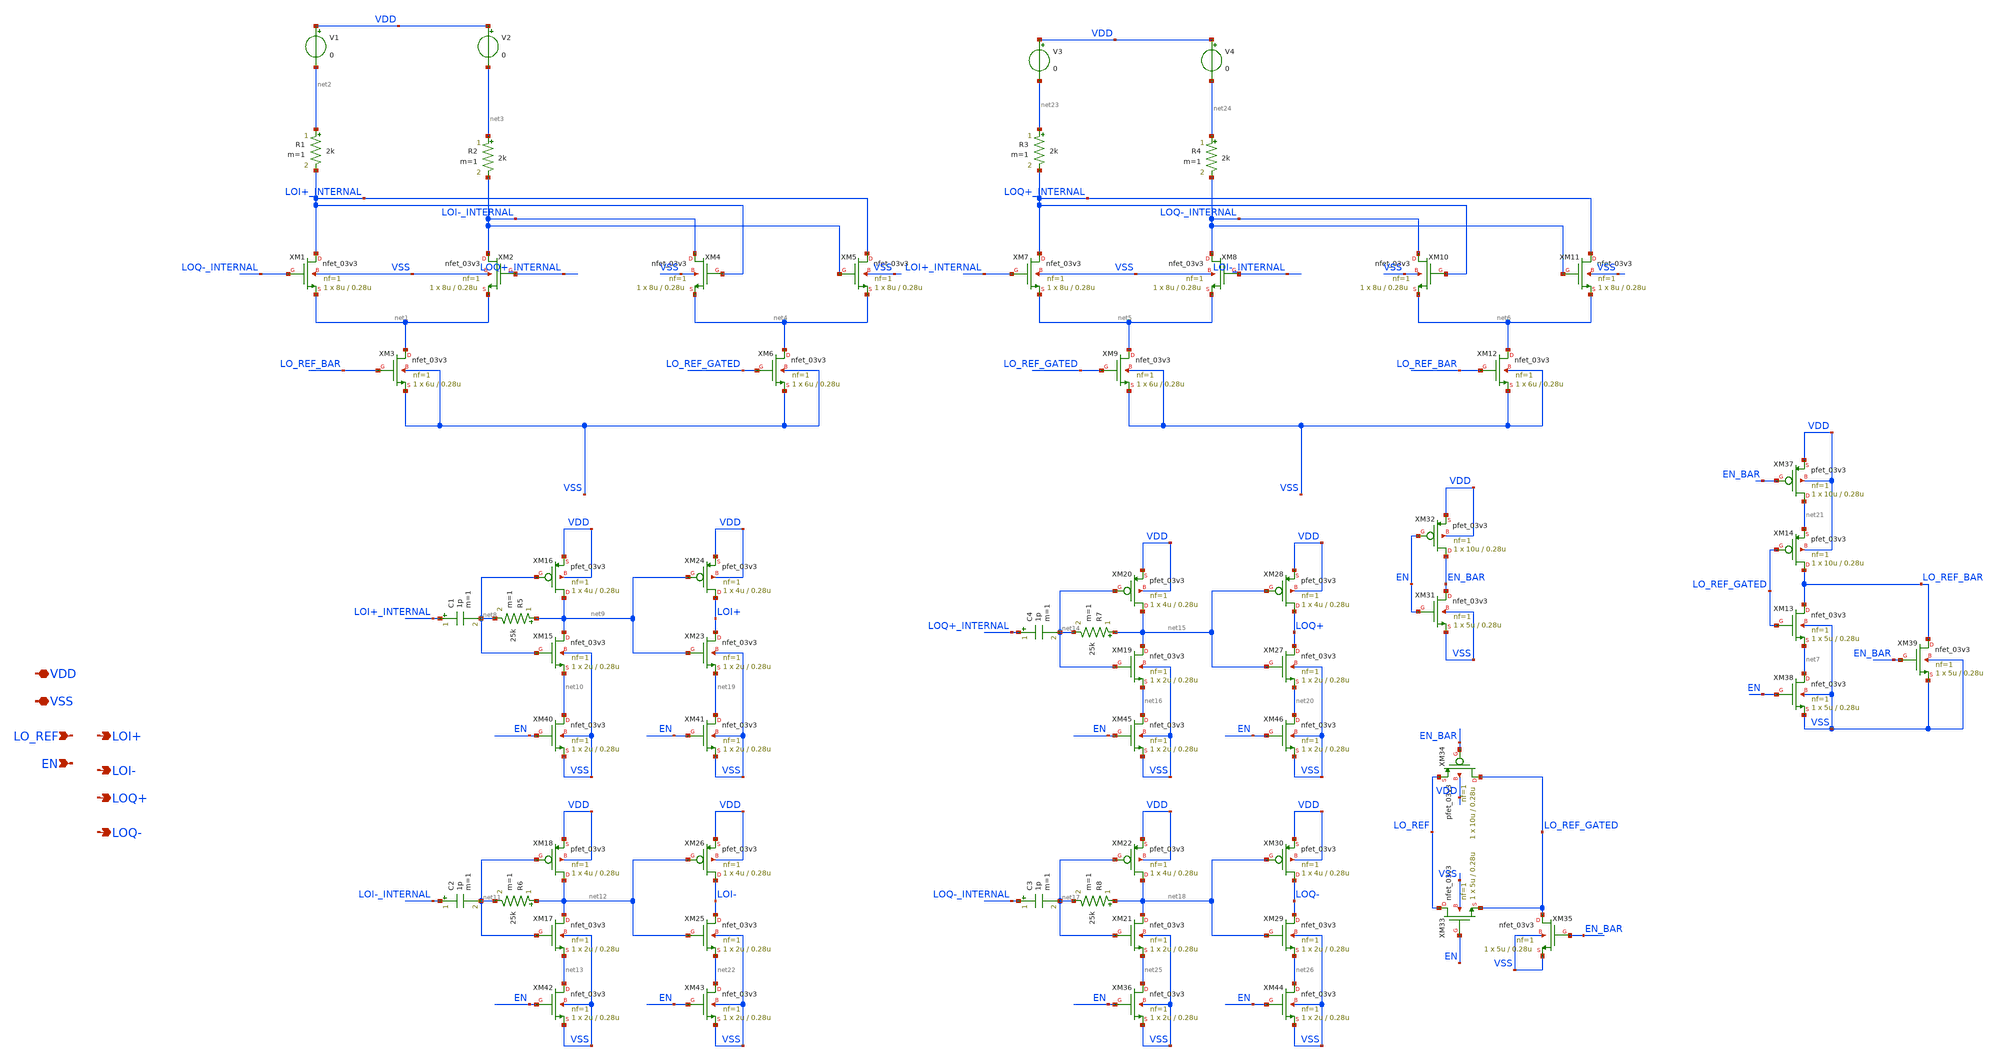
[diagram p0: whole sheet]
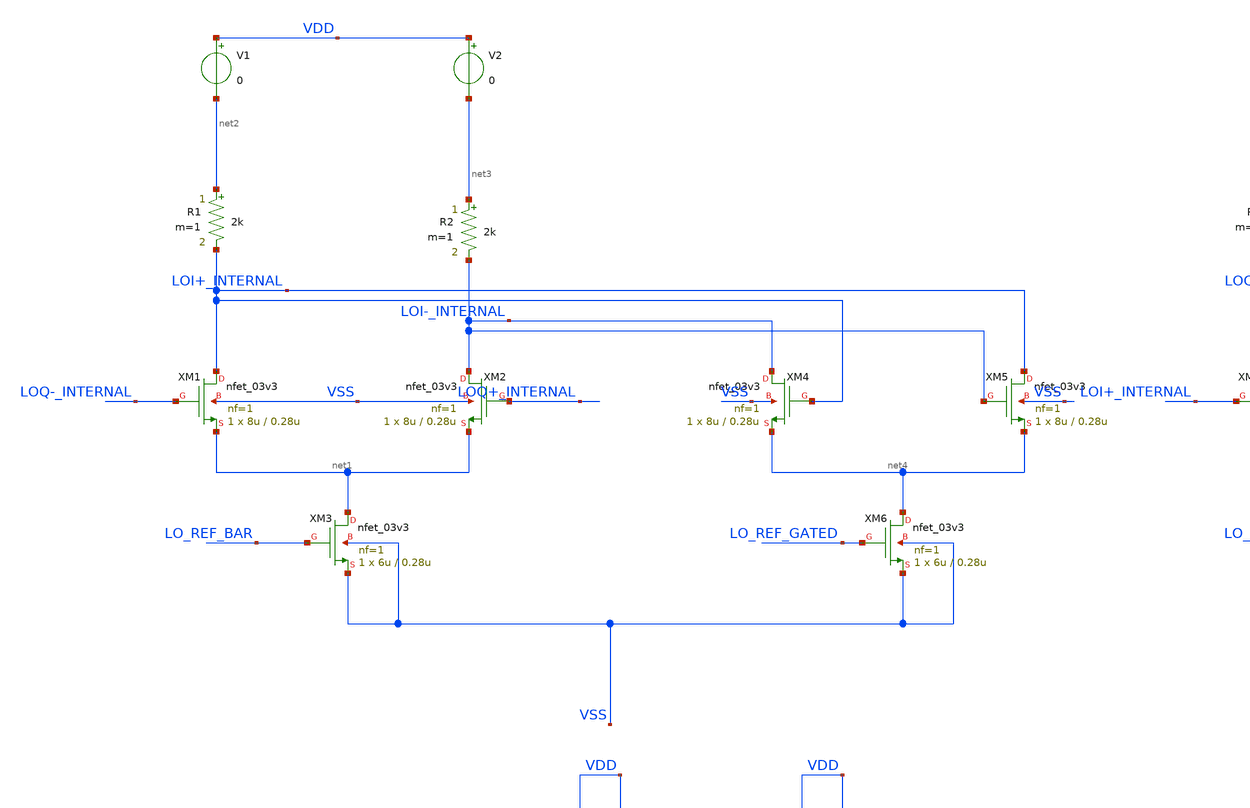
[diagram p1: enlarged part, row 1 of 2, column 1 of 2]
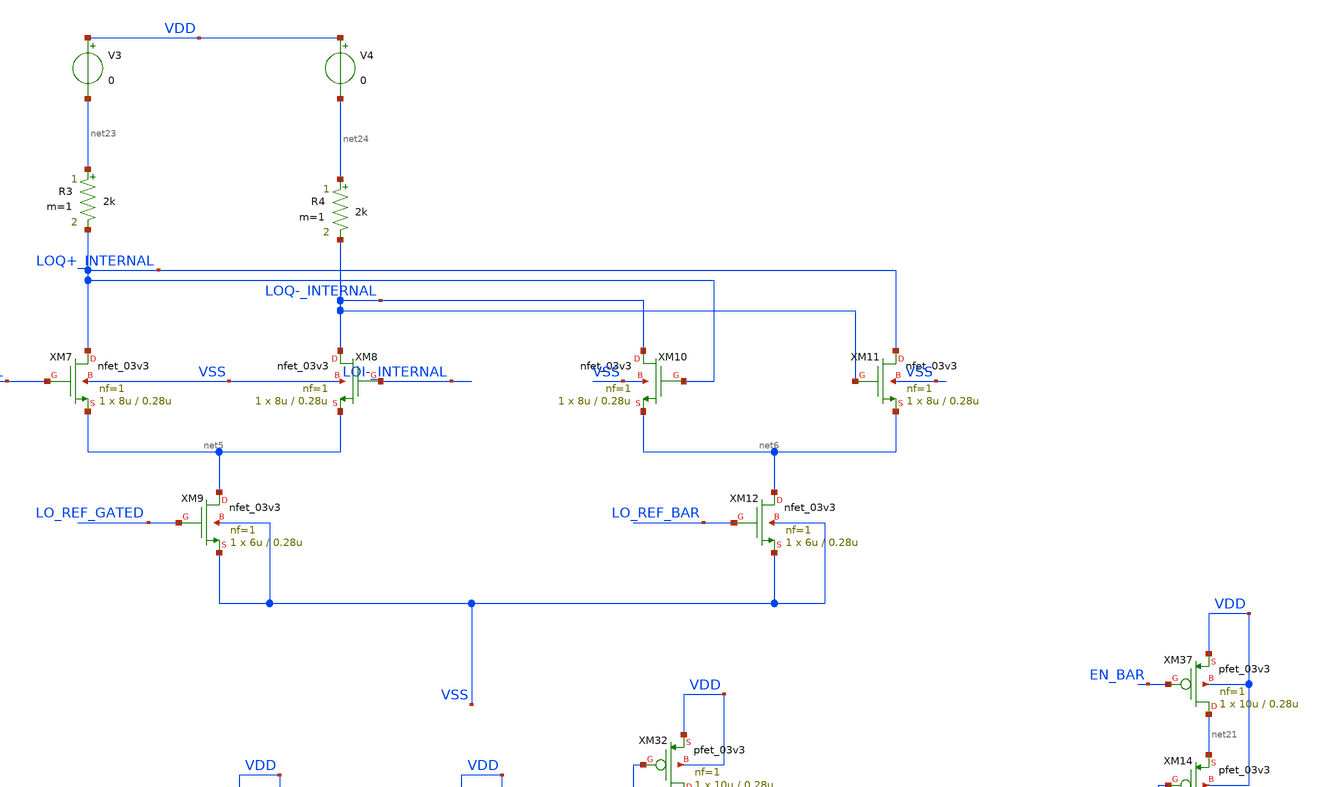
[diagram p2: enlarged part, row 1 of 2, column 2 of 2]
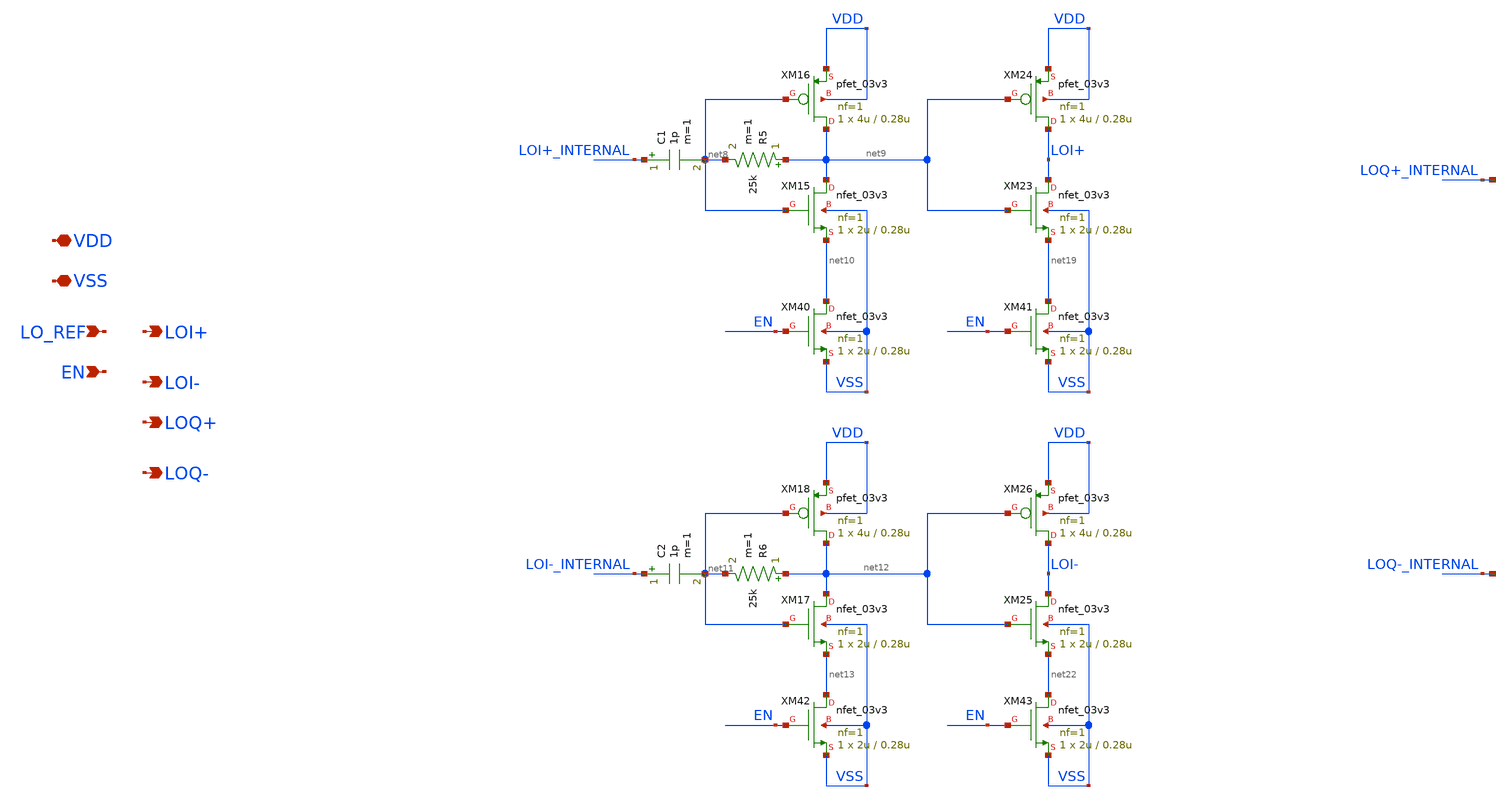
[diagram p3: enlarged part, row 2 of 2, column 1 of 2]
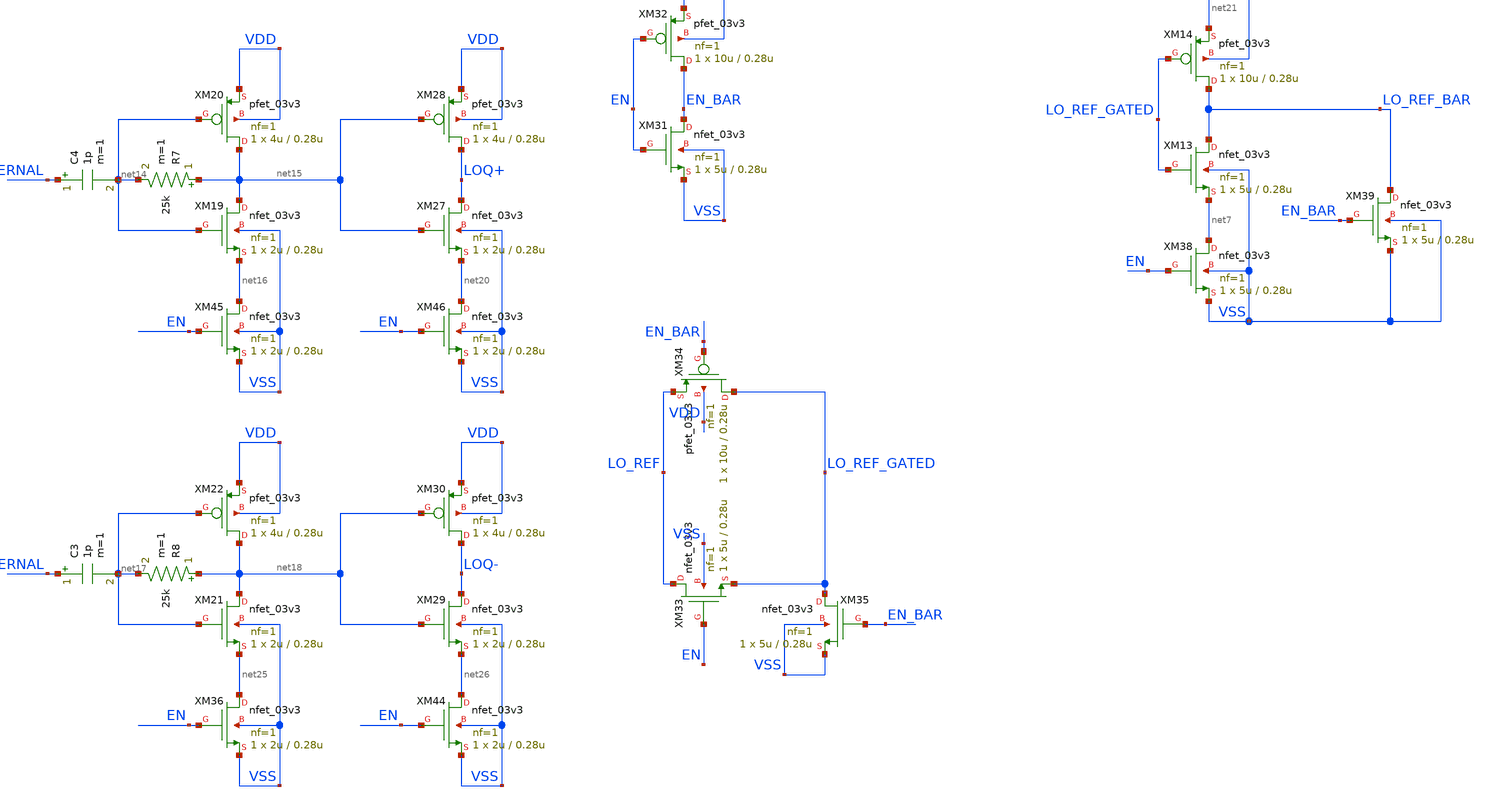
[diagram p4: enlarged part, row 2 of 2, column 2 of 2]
** sch_path: designs/divider/schematic/divider_ideal_passives.sch
**.subckt divider_ideal_passives VDD VSS LO_REF LOI+ LOI- LOQ+ LOQ- EN
*.iopin VDD
*.iopin VSS
*.ipin LO_REF
*.opin LOI+
*.opin LOI-
*.opin LOQ+
*.opin LOQ-
*.ipin EN
XM1 LOI+_INTERNAL LOQ-_INTERNAL net1 VSS nfet_03v3 L=0.28u W=8u nf=1 ad='int((nf+1)/2) * W/nf * 0.18u'
+ as='int((nf+2)/2) * W/nf * 0.18u' pd='2*int((nf+1)/2) * (W/nf + 0.18u)' ps='2*int((nf+2)/2) * (W/nf + 0.18u)'
+ nrd='0.18u / W' nrs='0.18u / W' sa=0 sb=0 sd=0 m=1
XM2 LOI-_INTERNAL LOQ+_INTERNAL net1 VSS nfet_03v3 L=0.28u W=8u nf=1 ad='int((nf+1)/2) * W/nf * 0.18u'
+ as='int((nf+2)/2) * W/nf * 0.18u' pd='2*int((nf+1)/2) * (W/nf + 0.18u)' ps='2*int((nf+2)/2) * (W/nf + 0.18u)'
+ nrd='0.18u / W' nrs='0.18u / W' sa=0 sb=0 sd=0 m=1
XM3 net1 LO_REF_BAR VSS VSS nfet_03v3 L=0.28u W=6u nf=1 ad='int((nf+1)/2) * W/nf * 0.18u' as='int((nf+2)/2) * W/nf * 0.18u'
+ pd='2*int((nf+1)/2) * (W/nf + 0.18u)' ps='2*int((nf+2)/2) * (W/nf + 0.18u)' nrd='0.18u / W' nrs='0.18u / W'
+ sa=0 sb=0 sd=0 m=1
R1 net2 LOI+_INTERNAL 2k m=1
R2 net3 LOI-_INTERNAL 2k m=1
XM4 LOI-_INTERNAL LOI+_INTERNAL net4 VSS nfet_03v3 L=0.28u W=8u nf=1 ad='int((nf+1)/2) * W/nf * 0.18u'
+ as='int((nf+2)/2) * W/nf * 0.18u' pd='2*int((nf+1)/2) * (W/nf + 0.18u)' ps='2*int((nf+2)/2) * (W/nf + 0.18u)'
+ nrd='0.18u / W' nrs='0.18u / W' sa=0 sb=0 sd=0 m=1
XM5 LOI+_INTERNAL LOI-_INTERNAL net4 VSS nfet_03v3 L=0.28u W=8u nf=1 ad='int((nf+1)/2) * W/nf * 0.18u'
+ as='int((nf+2)/2) * W/nf * 0.18u' pd='2*int((nf+1)/2) * (W/nf + 0.18u)' ps='2*int((nf+2)/2) * (W/nf + 0.18u)'
+ nrd='0.18u / W' nrs='0.18u / W' sa=0 sb=0 sd=0 m=1
XM6 net4 LO_REF_GATED VSS VSS nfet_03v3 L=0.28u W=6u nf=1 ad='int((nf+1)/2) * W/nf * 0.18u' as='int((nf+2)/2) * W/nf * 0.18u'
+ pd='2*int((nf+1)/2) * (W/nf + 0.18u)' ps='2*int((nf+2)/2) * (W/nf + 0.18u)' nrd='0.18u / W' nrs='0.18u / W'
+ sa=0 sb=0 sd=0 m=1
XM7 LOQ+_INTERNAL LOI+_INTERNAL net5 VSS nfet_03v3 L=0.28u W=8u nf=1 ad='int((nf+1)/2) * W/nf * 0.18u'
+ as='int((nf+2)/2) * W/nf * 0.18u' pd='2*int((nf+1)/2) * (W/nf + 0.18u)' ps='2*int((nf+2)/2) * (W/nf + 0.18u)'
+ nrd='0.18u / W' nrs='0.18u / W' sa=0 sb=0 sd=0 m=1
XM8 LOQ-_INTERNAL LOI-_INTERNAL net5 VSS nfet_03v3 L=0.28u W=8u nf=1 ad='int((nf+1)/2) * W/nf * 0.18u'
+ as='int((nf+2)/2) * W/nf * 0.18u' pd='2*int((nf+1)/2) * (W/nf + 0.18u)' ps='2*int((nf+2)/2) * (W/nf + 0.18u)'
+ nrd='0.18u / W' nrs='0.18u / W' sa=0 sb=0 sd=0 m=1
XM9 net5 LO_REF_GATED VSS VSS nfet_03v3 L=0.28u W=6u nf=1 ad='int((nf+1)/2) * W/nf * 0.18u' as='int((nf+2)/2) * W/nf * 0.18u'
+ pd='2*int((nf+1)/2) * (W/nf + 0.18u)' ps='2*int((nf+2)/2) * (W/nf + 0.18u)' nrd='0.18u / W' nrs='0.18u / W'
+ sa=0 sb=0 sd=0 m=1
R3 net23 LOQ+_INTERNAL 2k m=1
R4 net24 LOQ-_INTERNAL 2k m=1
XM10 LOQ-_INTERNAL LOQ+_INTERNAL net6 VSS nfet_03v3 L=0.28u W=8u nf=1 ad='int((nf+1)/2) * W/nf * 0.18u'
+ as='int((nf+2)/2) * W/nf * 0.18u' pd='2*int((nf+1)/2) * (W/nf + 0.18u)' ps='2*int((nf+2)/2) * (W/nf + 0.18u)'
+ nrd='0.18u / W' nrs='0.18u / W' sa=0 sb=0 sd=0 m=1
XM11 LOQ+_INTERNAL LOQ-_INTERNAL net6 VSS nfet_03v3 L=0.28u W=8u nf=1 ad='int((nf+1)/2) * W/nf * 0.18u'
+ as='int((nf+2)/2) * W/nf * 0.18u' pd='2*int((nf+1)/2) * (W/nf + 0.18u)' ps='2*int((nf+2)/2) * (W/nf + 0.18u)'
+ nrd='0.18u / W' nrs='0.18u / W' sa=0 sb=0 sd=0 m=1
XM12 net6 LO_REF_BAR VSS VSS nfet_03v3 L=0.28u W=6u nf=1 ad='int((nf+1)/2) * W/nf * 0.18u' as='int((nf+2)/2) * W/nf * 0.18u'
+ pd='2*int((nf+1)/2) * (W/nf + 0.18u)' ps='2*int((nf+2)/2) * (W/nf + 0.18u)' nrd='0.18u / W' nrs='0.18u / W'
+ sa=0 sb=0 sd=0 m=1
XM13 LO_REF_BAR LO_REF_GATED net7 VSS nfet_03v3 L=0.28u W=5u nf=1 ad='int((nf+1)/2) * W/nf * 0.18u' as='int((nf+2)/2) * W/nf * 0.18u'
+ pd='2*int((nf+1)/2) * (W/nf + 0.18u)' ps='2*int((nf+2)/2) * (W/nf + 0.18u)' nrd='0.18u / W' nrs='0.18u / W'
+ sa=0 sb=0 sd=0 m=1
XM14 LO_REF_BAR LO_REF_GATED net21 VDD pfet_03v3 L=0.28u W=10u nf=1 ad='int((nf+1)/2) * W/nf * 0.18u'
+ as='int((nf+2)/2) * W/nf * 0.18u' pd='2*int((nf+1)/2) * (W/nf + 0.18u)' ps='2*int((nf+2)/2) * (W/nf + 0.18u)'
+ nrd='0.18u / W' nrs='0.18u / W' sa=0 sb=0 sd=0 m=1
V1 VDD net2 0
V2 VDD net3 0
XM15 net9 net8 net10 VSS nfet_03v3 L=0.28u W=2u nf=1 ad='int((nf+1)/2) * W/nf * 0.18u' as='int((nf+2)/2) * W/nf * 0.18u'
+ pd='2*int((nf+1)/2) * (W/nf + 0.18u)' ps='2*int((nf+2)/2) * (W/nf + 0.18u)' nrd='0.18u / W' nrs='0.18u / W'
+ sa=0 sb=0 sd=0 m=1
XM16 net9 net8 VDD VDD pfet_03v3 L=0.28u W=4u nf=1 ad='int((nf+1)/2) * W/nf * 0.18u' as='int((nf+2)/2) * W/nf * 0.18u'
+ pd='2*int((nf+1)/2) * (W/nf + 0.18u)' ps='2*int((nf+2)/2) * (W/nf + 0.18u)' nrd='0.18u / W' nrs='0.18u / W'
+ sa=0 sb=0 sd=0 m=1
R5 net9 net8 25k m=1
XM17 net12 net11 net13 VSS nfet_03v3 L=0.28u W=2u nf=1 ad='int((nf+1)/2) * W/nf * 0.18u' as='int((nf+2)/2) * W/nf * 0.18u'
+ pd='2*int((nf+1)/2) * (W/nf + 0.18u)' ps='2*int((nf+2)/2) * (W/nf + 0.18u)' nrd='0.18u / W' nrs='0.18u / W'
+ sa=0 sb=0 sd=0 m=1
XM18 net12 net11 VDD VDD pfet_03v3 L=0.28u W=4u nf=1 ad='int((nf+1)/2) * W/nf * 0.18u' as='int((nf+2)/2) * W/nf * 0.18u'
+ pd='2*int((nf+1)/2) * (W/nf + 0.18u)' ps='2*int((nf+2)/2) * (W/nf + 0.18u)' nrd='0.18u / W' nrs='0.18u / W'
+ sa=0 sb=0 sd=0 m=1
R6 net12 net11 25k m=1
XM19 net15 net14 net16 VSS nfet_03v3 L=0.28u W=2u nf=1 ad='int((nf+1)/2) * W/nf * 0.18u' as='int((nf+2)/2) * W/nf * 0.18u'
+ pd='2*int((nf+1)/2) * (W/nf + 0.18u)' ps='2*int((nf+2)/2) * (W/nf + 0.18u)' nrd='0.18u / W' nrs='0.18u / W'
+ sa=0 sb=0 sd=0 m=1
XM20 net15 net14 VDD VDD pfet_03v3 L=0.28u W=4u nf=1 ad='int((nf+1)/2) * W/nf * 0.18u' as='int((nf+2)/2) * W/nf * 0.18u'
+ pd='2*int((nf+1)/2) * (W/nf + 0.18u)' ps='2*int((nf+2)/2) * (W/nf + 0.18u)' nrd='0.18u / W' nrs='0.18u / W'
+ sa=0 sb=0 sd=0 m=1
R7 net15 net14 25k m=1
XM21 net18 net17 net25 VSS nfet_03v3 L=0.28u W=2u nf=1 ad='int((nf+1)/2) * W/nf * 0.18u' as='int((nf+2)/2) * W/nf * 0.18u'
+ pd='2*int((nf+1)/2) * (W/nf + 0.18u)' ps='2*int((nf+2)/2) * (W/nf + 0.18u)' nrd='0.18u / W' nrs='0.18u / W'
+ sa=0 sb=0 sd=0 m=1
XM22 net18 net17 VDD VDD pfet_03v3 L=0.28u W=4u nf=1 ad='int((nf+1)/2) * W/nf * 0.18u' as='int((nf+2)/2) * W/nf * 0.18u'
+ pd='2*int((nf+1)/2) * (W/nf + 0.18u)' ps='2*int((nf+2)/2) * (W/nf + 0.18u)' nrd='0.18u / W' nrs='0.18u / W'
+ sa=0 sb=0 sd=0 m=1
R8 net18 net17 25k m=1
C1 LOI+_INTERNAL net8 1p m=1
C2 LOI-_INTERNAL net11 1p m=1
C3 LOQ-_INTERNAL net17 1p m=1
C4 LOQ+_INTERNAL net14 1p m=1
XM23 LOI+ net9 net19 VSS nfet_03v3 L=0.28u W=2u nf=1 ad='int((nf+1)/2) * W/nf * 0.18u' as='int((nf+2)/2) * W/nf * 0.18u'
+ pd='2*int((nf+1)/2) * (W/nf + 0.18u)' ps='2*int((nf+2)/2) * (W/nf + 0.18u)' nrd='0.18u / W' nrs='0.18u / W'
+ sa=0 sb=0 sd=0 m=1
XM24 LOI+ net9 VDD VDD pfet_03v3 L=0.28u W=4u nf=1 ad='int((nf+1)/2) * W/nf * 0.18u' as='int((nf+2)/2) * W/nf * 0.18u'
+ pd='2*int((nf+1)/2) * (W/nf + 0.18u)' ps='2*int((nf+2)/2) * (W/nf + 0.18u)' nrd='0.18u / W' nrs='0.18u / W'
+ sa=0 sb=0 sd=0 m=1
XM25 LOI- net12 net22 VSS nfet_03v3 L=0.28u W=2u nf=1 ad='int((nf+1)/2) * W/nf * 0.18u' as='int((nf+2)/2) * W/nf * 0.18u'
+ pd='2*int((nf+1)/2) * (W/nf + 0.18u)' ps='2*int((nf+2)/2) * (W/nf + 0.18u)' nrd='0.18u / W' nrs='0.18u / W'
+ sa=0 sb=0 sd=0 m=1
XM26 LOI- net12 VDD VDD pfet_03v3 L=0.28u W=4u nf=1 ad='int((nf+1)/2) * W/nf * 0.18u' as='int((nf+2)/2) * W/nf * 0.18u'
+ pd='2*int((nf+1)/2) * (W/nf + 0.18u)' ps='2*int((nf+2)/2) * (W/nf + 0.18u)' nrd='0.18u / W' nrs='0.18u / W'
+ sa=0 sb=0 sd=0 m=1
XM27 LOQ+ net15 net20 VSS nfet_03v3 L=0.28u W=2u nf=1 ad='int((nf+1)/2) * W/nf * 0.18u' as='int((nf+2)/2) * W/nf * 0.18u'
+ pd='2*int((nf+1)/2) * (W/nf + 0.18u)' ps='2*int((nf+2)/2) * (W/nf + 0.18u)' nrd='0.18u / W' nrs='0.18u / W'
+ sa=0 sb=0 sd=0 m=1
XM28 LOQ+ net15 VDD VDD pfet_03v3 L=0.28u W=4u nf=1 ad='int((nf+1)/2) * W/nf * 0.18u' as='int((nf+2)/2) * W/nf * 0.18u'
+ pd='2*int((nf+1)/2) * (W/nf + 0.18u)' ps='2*int((nf+2)/2) * (W/nf + 0.18u)' nrd='0.18u / W' nrs='0.18u / W'
+ sa=0 sb=0 sd=0 m=1
XM29 LOQ- net18 net26 VSS nfet_03v3 L=0.28u W=2u nf=1 ad='int((nf+1)/2) * W/nf * 0.18u' as='int((nf+2)/2) * W/nf * 0.18u'
+ pd='2*int((nf+1)/2) * (W/nf + 0.18u)' ps='2*int((nf+2)/2) * (W/nf + 0.18u)' nrd='0.18u / W' nrs='0.18u / W'
+ sa=0 sb=0 sd=0 m=1
XM30 LOQ- net18 VDD VDD pfet_03v3 L=0.28u W=4u nf=1 ad='int((nf+1)/2) * W/nf * 0.18u' as='int((nf+2)/2) * W/nf * 0.18u'
+ pd='2*int((nf+1)/2) * (W/nf + 0.18u)' ps='2*int((nf+2)/2) * (W/nf + 0.18u)' nrd='0.18u / W' nrs='0.18u / W'
+ sa=0 sb=0 sd=0 m=1
XM31 EN_BAR EN VSS VSS nfet_03v3 L=0.28u W=5u nf=1 ad='int((nf+1)/2) * W/nf * 0.18u' as='int((nf+2)/2) * W/nf * 0.18u'
+ pd='2*int((nf+1)/2) * (W/nf + 0.18u)' ps='2*int((nf+2)/2) * (W/nf + 0.18u)' nrd='0.18u / W' nrs='0.18u / W'
+ sa=0 sb=0 sd=0 m=1
XM32 EN_BAR EN VDD VDD pfet_03v3 L=0.28u W=10u nf=1 ad='int((nf+1)/2) * W/nf * 0.18u' as='int((nf+2)/2) * W/nf * 0.18u'
+ pd='2*int((nf+1)/2) * (W/nf + 0.18u)' ps='2*int((nf+2)/2) * (W/nf + 0.18u)' nrd='0.18u / W' nrs='0.18u / W'
+ sa=0 sb=0 sd=0 m=1
XM33 LO_REF EN LO_REF_GATED VSS nfet_03v3 L=0.28u W=5u nf=1 ad='int((nf+1)/2) * W/nf * 0.18u' as='int((nf+2)/2) * W/nf * 0.18u'
+ pd='2*int((nf+1)/2) * (W/nf + 0.18u)' ps='2*int((nf+2)/2) * (W/nf + 0.18u)' nrd='0.18u / W' nrs='0.18u / W'
+ sa=0 sb=0 sd=0 m=1
XM34 LO_REF_GATED EN_BAR LO_REF VDD pfet_03v3 L=0.28u W=10u nf=1 ad='int((nf+1)/2) * W/nf * 0.18u' as='int((nf+2)/2) * W/nf * 0.18u'
+ pd='2*int((nf+1)/2) * (W/nf + 0.18u)' ps='2*int((nf+2)/2) * (W/nf + 0.18u)' nrd='0.18u / W' nrs='0.18u / W'
+ sa=0 sb=0 sd=0 m=1
XM35 LO_REF_GATED EN_BAR VSS VSS nfet_03v3 L=0.28u W=5u nf=1 ad='int((nf+1)/2) * W/nf * 0.18u' as='int((nf+2)/2) * W/nf * 0.18u'
+ pd='2*int((nf+1)/2) * (W/nf + 0.18u)' ps='2*int((nf+2)/2) * (W/nf + 0.18u)' nrd='0.18u / W' nrs='0.18u / W'
+ sa=0 sb=0 sd=0 m=1
XM37 net21 EN_BAR VDD VDD pfet_03v3 L=0.28u W=10u nf=1 ad='int((nf+1)/2) * W/nf * 0.18u' as='int((nf+2)/2) * W/nf * 0.18u'
+ pd='2*int((nf+1)/2) * (W/nf + 0.18u)' ps='2*int((nf+2)/2) * (W/nf + 0.18u)' nrd='0.18u / W' nrs='0.18u / W'
+ sa=0 sb=0 sd=0 m=1
XM38 net7 EN VSS VSS nfet_03v3 L=0.28u W=5u nf=1 ad='int((nf+1)/2) * W/nf * 0.18u' as='int((nf+2)/2) * W/nf * 0.18u'
+ pd='2*int((nf+1)/2) * (W/nf + 0.18u)' ps='2*int((nf+2)/2) * (W/nf + 0.18u)' nrd='0.18u / W' nrs='0.18u / W'
+ sa=0 sb=0 sd=0 m=1
XM39 LO_REF_BAR EN_BAR VSS VSS nfet_03v3 L=0.28u W=5u nf=1 ad='int((nf+1)/2) * W/nf * 0.18u' as='int((nf+2)/2) * W/nf * 0.18u'
+ pd='2*int((nf+1)/2) * (W/nf + 0.18u)' ps='2*int((nf+2)/2) * (W/nf + 0.18u)' nrd='0.18u / W' nrs='0.18u / W'
+ sa=0 sb=0 sd=0 m=1
XM40 net10 EN VSS VSS nfet_03v3 L=0.28u W=2u nf=1 ad='int((nf+1)/2) * W/nf * 0.18u' as='int((nf+2)/2) * W/nf * 0.18u'
+ pd='2*int((nf+1)/2) * (W/nf + 0.18u)' ps='2*int((nf+2)/2) * (W/nf + 0.18u)' nrd='0.18u / W' nrs='0.18u / W'
+ sa=0 sb=0 sd=0 m=1
XM41 net19 EN VSS VSS nfet_03v3 L=0.28u W=2u nf=1 ad='int((nf+1)/2) * W/nf * 0.18u' as='int((nf+2)/2) * W/nf * 0.18u'
+ pd='2*int((nf+1)/2) * (W/nf + 0.18u)' ps='2*int((nf+2)/2) * (W/nf + 0.18u)' nrd='0.18u / W' nrs='0.18u / W'
+ sa=0 sb=0 sd=0 m=1
XM42 net13 EN VSS VSS nfet_03v3 L=0.28u W=2u nf=1 ad='int((nf+1)/2) * W/nf * 0.18u' as='int((nf+2)/2) * W/nf * 0.18u'
+ pd='2*int((nf+1)/2) * (W/nf + 0.18u)' ps='2*int((nf+2)/2) * (W/nf + 0.18u)' nrd='0.18u / W' nrs='0.18u / W'
+ sa=0 sb=0 sd=0 m=1
XM43 net22 EN VSS VSS nfet_03v3 L=0.28u W=2u nf=1 ad='int((nf+1)/2) * W/nf * 0.18u' as='int((nf+2)/2) * W/nf * 0.18u'
+ pd='2*int((nf+1)/2) * (W/nf + 0.18u)' ps='2*int((nf+2)/2) * (W/nf + 0.18u)' nrd='0.18u / W' nrs='0.18u / W'
+ sa=0 sb=0 sd=0 m=1
V3 VDD net23 0
V4 VDD net24 0
XM36 net25 EN VSS VSS nfet_03v3 L=0.28u W=2u nf=1 ad='int((nf+1)/2) * W/nf * 0.18u' as='int((nf+2)/2) * W/nf * 0.18u'
+ pd='2*int((nf+1)/2) * (W/nf + 0.18u)' ps='2*int((nf+2)/2) * (W/nf + 0.18u)' nrd='0.18u / W' nrs='0.18u / W'
+ sa=0 sb=0 sd=0 m=1
XM44 net26 EN VSS VSS nfet_03v3 L=0.28u W=2u nf=1 ad='int((nf+1)/2) * W/nf * 0.18u' as='int((nf+2)/2) * W/nf * 0.18u'
+ pd='2*int((nf+1)/2) * (W/nf + 0.18u)' ps='2*int((nf+2)/2) * (W/nf + 0.18u)' nrd='0.18u / W' nrs='0.18u / W'
+ sa=0 sb=0 sd=0 m=1
XM45 net16 EN VSS VSS nfet_03v3 L=0.28u W=2u nf=1 ad='int((nf+1)/2) * W/nf * 0.18u' as='int((nf+2)/2) * W/nf * 0.18u'
+ pd='2*int((nf+1)/2) * (W/nf + 0.18u)' ps='2*int((nf+2)/2) * (W/nf + 0.18u)' nrd='0.18u / W' nrs='0.18u / W'
+ sa=0 sb=0 sd=0 m=1
XM46 net20 EN VSS VSS nfet_03v3 L=0.28u W=2u nf=1 ad='int((nf+1)/2) * W/nf * 0.18u' as='int((nf+2)/2) * W/nf * 0.18u'
+ pd='2*int((nf+1)/2) * (W/nf + 0.18u)' ps='2*int((nf+2)/2) * (W/nf + 0.18u)' nrd='0.18u / W' nrs='0.18u / W'
+ sa=0 sb=0 sd=0 m=1
**.ends
.end
